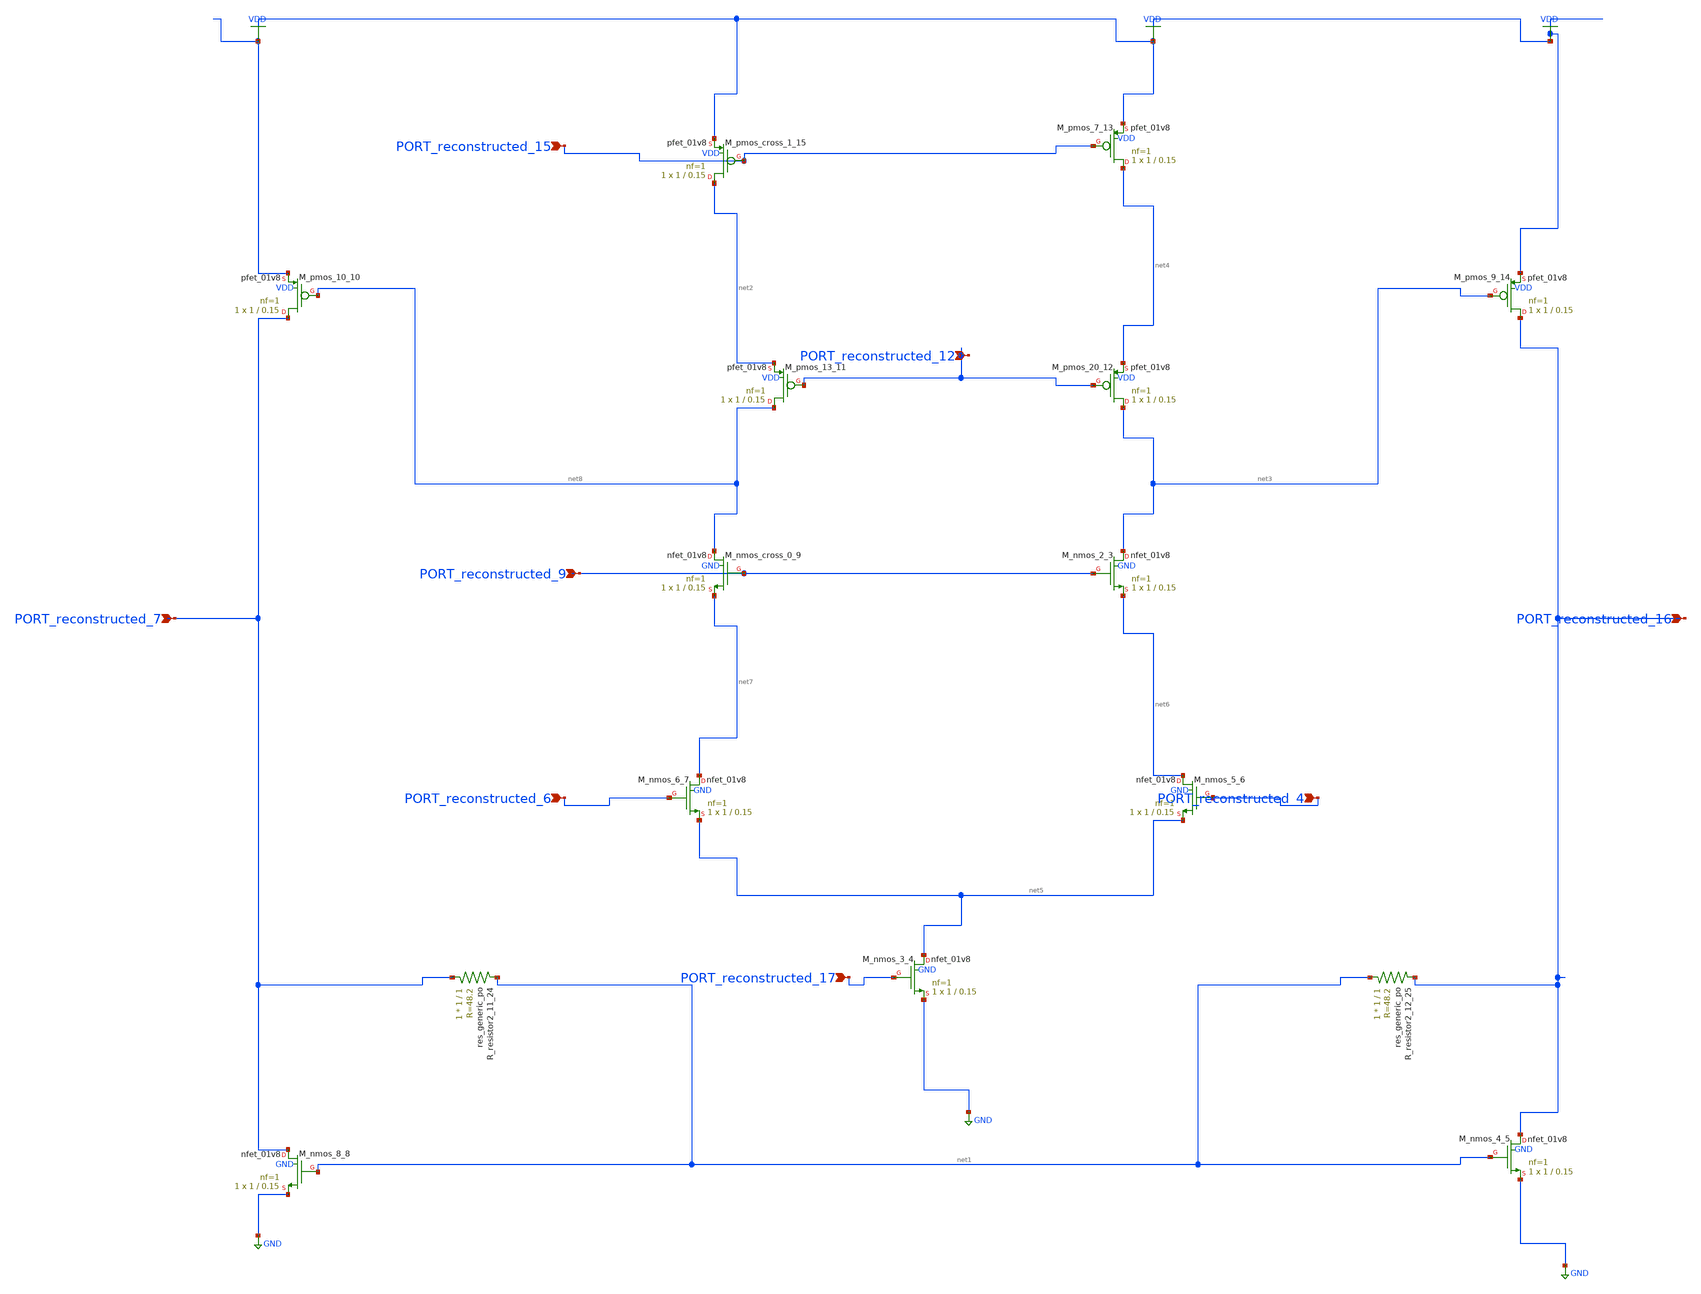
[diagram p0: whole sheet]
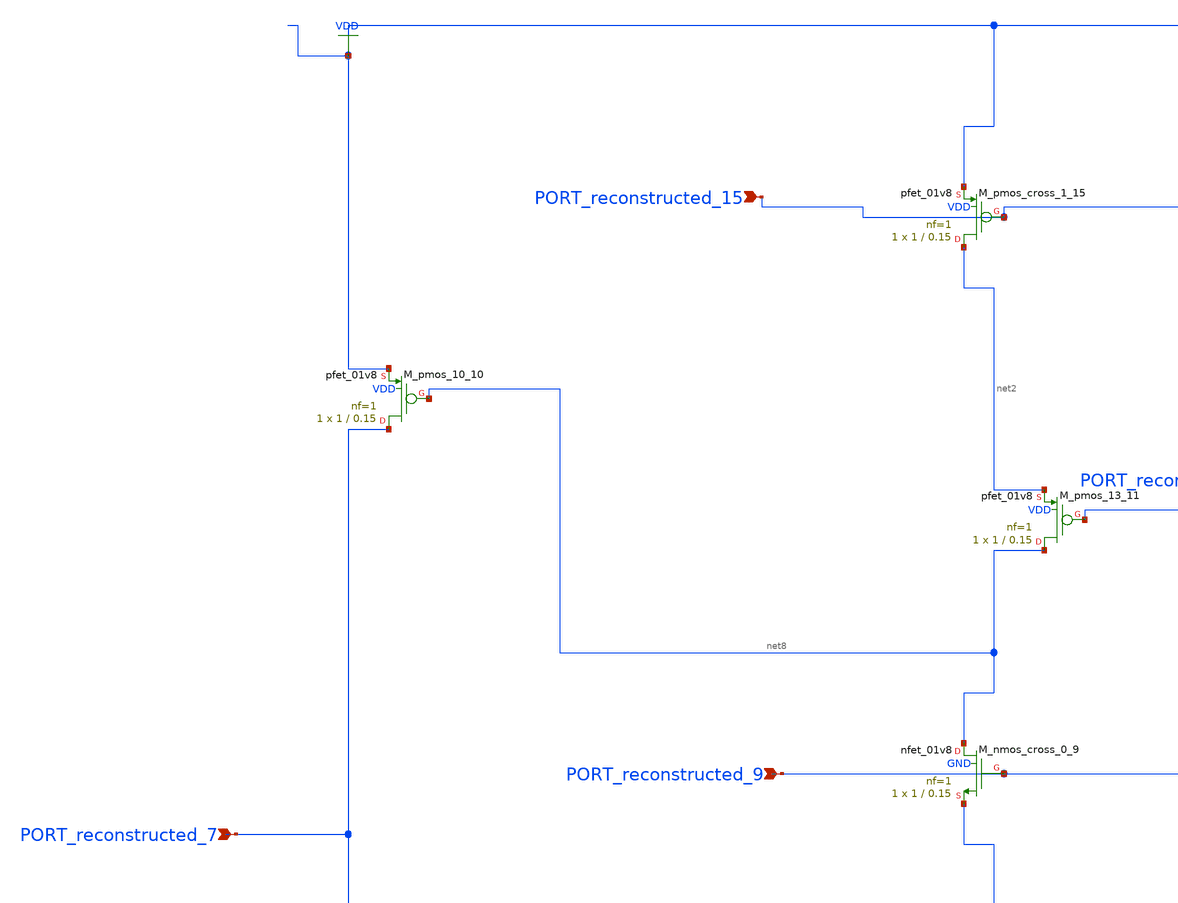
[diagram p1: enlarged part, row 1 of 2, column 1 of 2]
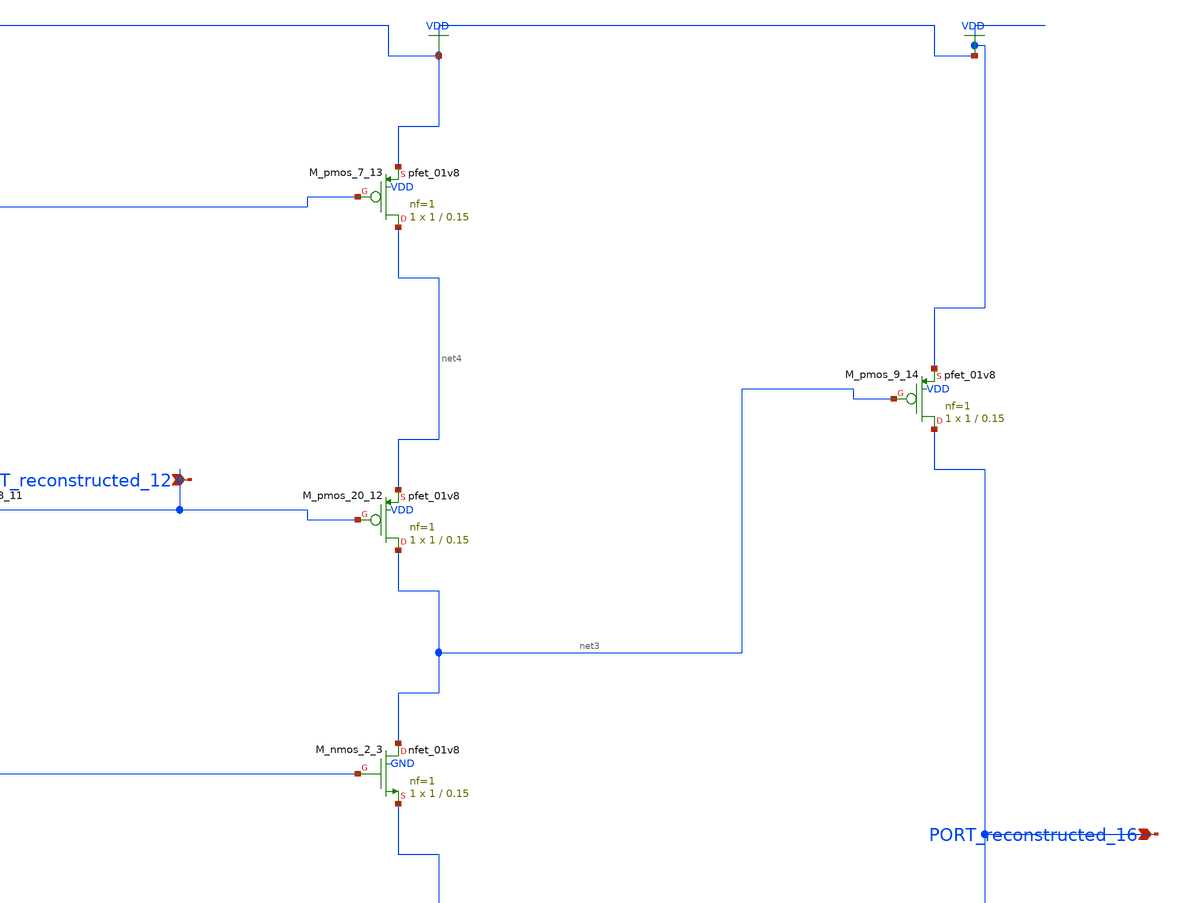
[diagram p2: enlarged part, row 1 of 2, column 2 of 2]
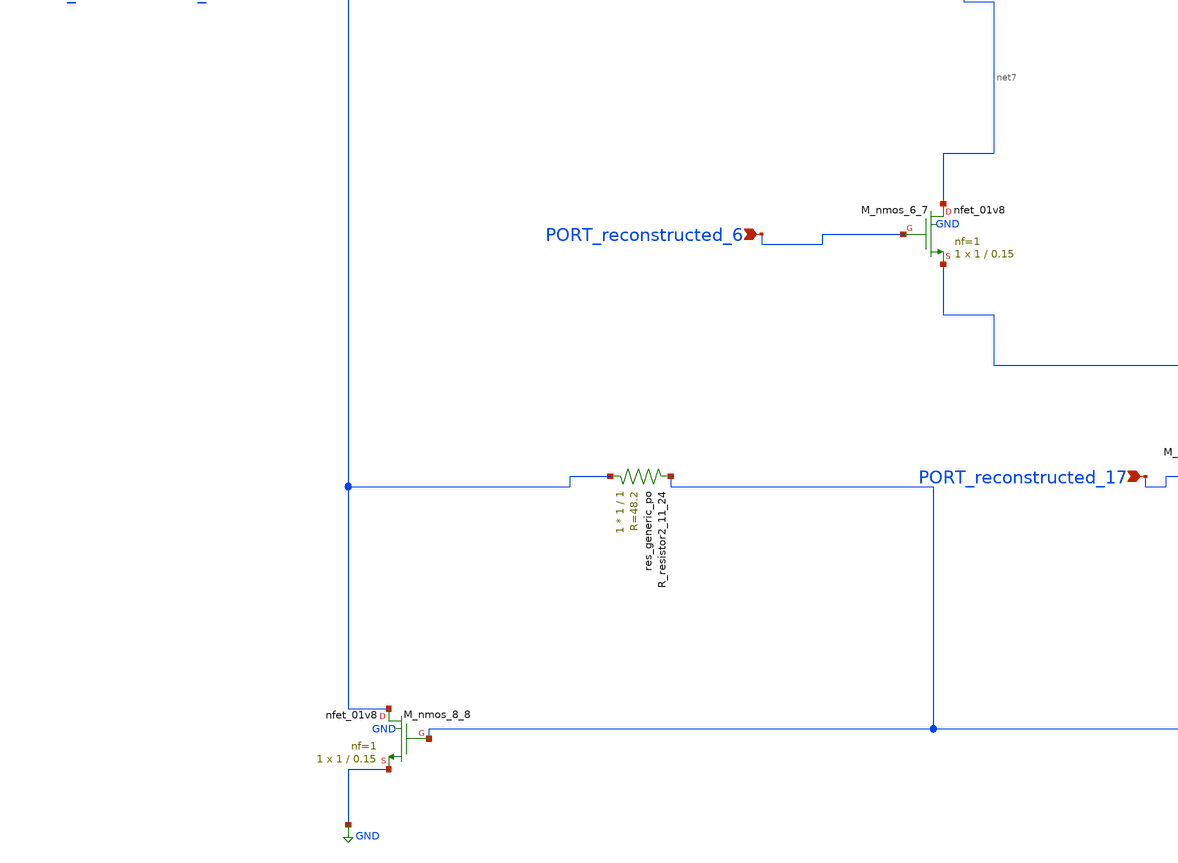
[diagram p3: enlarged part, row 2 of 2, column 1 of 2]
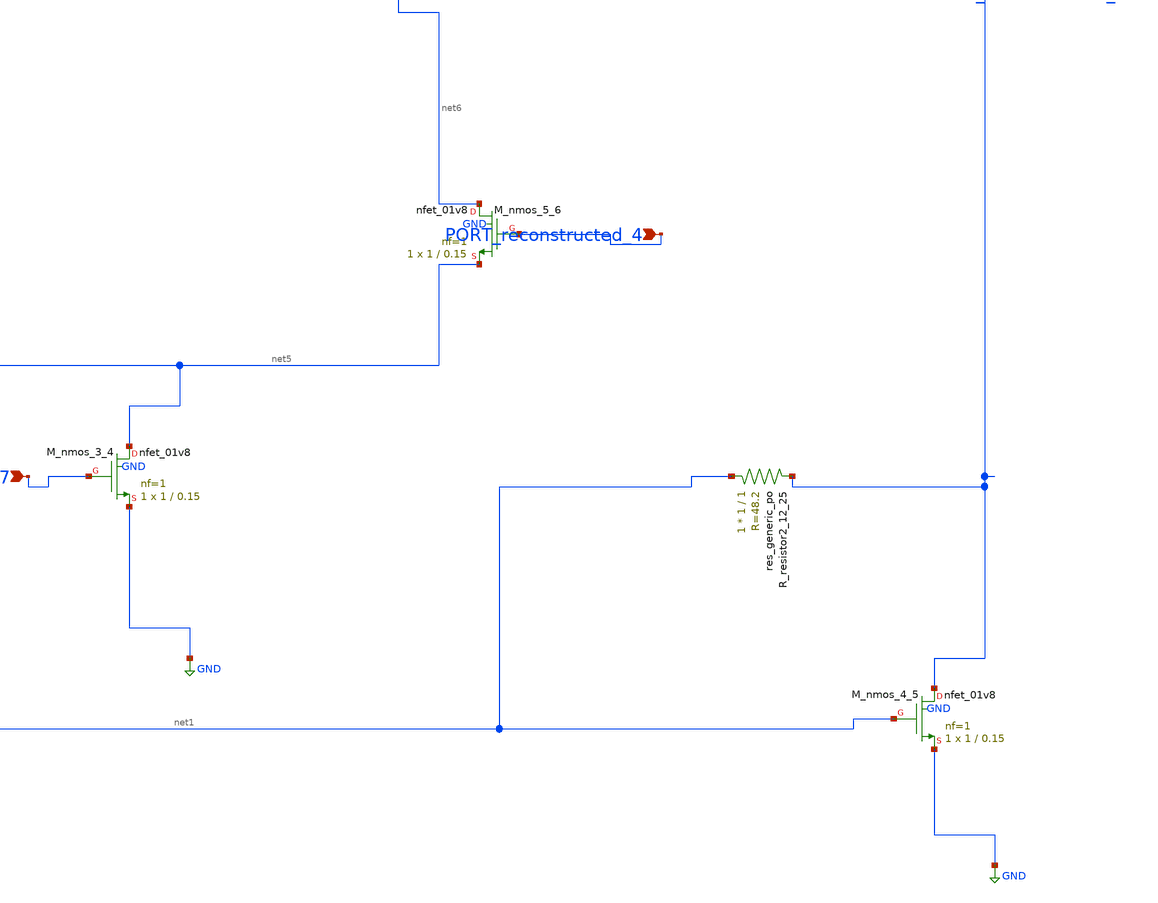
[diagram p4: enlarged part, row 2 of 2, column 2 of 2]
** sch_path: schematics/AMSNet/755.sch
**.subckt 755 PORT_reconstructed_4 PORT_reconstructed_16 PORT_reconstructed_7 PORT_reconstructed_6
*+ PORT_reconstructed_17 PORT_reconstructed_15 PORT_reconstructed_9 PORT_reconstructed_12
*.ipin PORT_reconstructed_4
*.ipin PORT_reconstructed_16
*.ipin PORT_reconstructed_7
*.ipin PORT_reconstructed_6
*.ipin PORT_reconstructed_17
*.ipin PORT_reconstructed_15
*.ipin PORT_reconstructed_9
*.ipin PORT_reconstructed_12
XM_nmos_2_3 net3 PORT_reconstructed_9 net6 GND sky130_fd_pr__nfet_01v8 L=0.15 W=1 nf=1 ad='int((1 + 1)/2) * 1 / 1 * 0.29'
+ as='int((1 + 2)/2) * 1 / 1 * 0.29' pd='2*int((1 + 1)/2) * (1 / 1 + 0.29)' ps='2*int((1 + 2)/2) * (1 / 1 + 0.29)'
+ nrd='0.29 / 1 ' nrs='0.29 / 1 ' sa=0 sb=0 sd=0 mult=1 m=1
XM_nmos_3_4 net5 PORT_reconstructed_17 GND GND sky130_fd_pr__nfet_01v8 L=0.15 W=1 nf=1 ad='int((1 + 1)/2) * 1 / 1 * 0.29'
+ as='int((1 + 2)/2) * 1 / 1 * 0.29' pd='2*int((1 + 1)/2) * (1 / 1 + 0.29)' ps='2*int((1 + 2)/2) * (1 / 1 + 0.29)'
+ nrd='0.29 / 1 ' nrs='0.29 / 1 ' sa=0 sb=0 sd=0 mult=1 m=1
XM_nmos_4_5 PORT_reconstructed_16 net1 GND GND sky130_fd_pr__nfet_01v8 L=0.15 W=1 nf=1 ad='int((1 + 1)/2) * 1 / 1 * 0.29'
+ as='int((1 + 2)/2) * 1 / 1 * 0.29' pd='2*int((1 + 1)/2) * (1 / 1 + 0.29)' ps='2*int((1 + 2)/2) * (1 / 1 + 0.29)'
+ nrd='0.29 / 1 ' nrs='0.29 / 1 ' sa=0 sb=0 sd=0 mult=1 m=1
XM_nmos_5_6 net6 PORT_reconstructed_4 net5 GND sky130_fd_pr__nfet_01v8 L=0.15 W=1 nf=1 ad='int((1 + 1)/2) * 1 / 1 * 0.29'
+ as='int((1 + 2)/2) * 1 / 1 * 0.29' pd='2*int((1 + 1)/2) * (1 / 1 + 0.29)' ps='2*int((1 + 2)/2) * (1 / 1 + 0.29)'
+ nrd='0.29 / 1 ' nrs='0.29 / 1 ' sa=0 sb=0 sd=0 mult=1 m=1
XM_nmos_6_7 net7 PORT_reconstructed_6 net5 GND sky130_fd_pr__nfet_01v8 L=0.15 W=1 nf=1 ad='int((1 + 1)/2) * 1 / 1 * 0.29'
+ as='int((1 + 2)/2) * 1 / 1 * 0.29' pd='2*int((1 + 1)/2) * (1 / 1 + 0.29)' ps='2*int((1 + 2)/2) * (1 / 1 + 0.29)'
+ nrd='0.29 / 1 ' nrs='0.29 / 1 ' sa=0 sb=0 sd=0 mult=1 m=1
XM_nmos_8_8 PORT_reconstructed_7 net1 GND GND sky130_fd_pr__nfet_01v8 L=0.15 W=1 nf=1 ad='int((1 + 1)/2) * 1 / 1 * 0.29'
+ as='int((1 + 2)/2) * 1 / 1 * 0.29' pd='2*int((1 + 1)/2) * (1 / 1 + 0.29)' ps='2*int((1 + 2)/2) * (1 / 1 + 0.29)'
+ nrd='0.29 / 1 ' nrs='0.29 / 1 ' sa=0 sb=0 sd=0 mult=1 m=1
XM_nmos_cross_0_9 net8 PORT_reconstructed_9 net7 GND sky130_fd_pr__nfet_01v8 L=0.15 W=1 nf=1 ad='int((1 + 1)/2) * 1 / 1 * 0.29'
+ as='int((1 + 2)/2) * 1 / 1 * 0.29' pd='2*int((1 + 1)/2) * (1 / 1 + 0.29)' ps='2*int((1 + 2)/2) * (1 / 1 + 0.29)'
+ nrd='0.29 / 1 ' nrs='0.29 / 1 ' sa=0 sb=0 sd=0 mult=1 m=1
XM_pmos_10_10 PORT_reconstructed_7 net8 VDD VDD sky130_fd_pr__pfet_01v8 L=0.15 W=1 nf=1 ad='int((1 + 1)/2) * 1 / 1 * 0.29'
+ as='int((1 + 2)/2) * 1 / 1 * 0.29' pd='2*int((1 + 1)/2) * (1 / 1 + 0.29)' ps='2*int((1 + 2)/2) * (1 / 1 + 0.29)'
+ nrd='0.29 / 1 ' nrs='0.29 / 1 ' sa=0 sb=0 sd=0 mult=1 m=1
XM_pmos_13_11 net8 PORT_reconstructed_12 net2 VDD sky130_fd_pr__pfet_01v8 L=0.15 W=1 nf=1 ad='int((1 + 1)/2) * 1 / 1 * 0.29'
+ as='int((1 + 2)/2) * 1 / 1 * 0.29' pd='2*int((1 + 1)/2) * (1 / 1 + 0.29)' ps='2*int((1 + 2)/2) * (1 / 1 + 0.29)'
+ nrd='0.29 / 1 ' nrs='0.29 / 1 ' sa=0 sb=0 sd=0 mult=1 m=1
XM_pmos_20_12 net3 PORT_reconstructed_12 net4 VDD sky130_fd_pr__pfet_01v8 L=0.15 W=1 nf=1 ad='int((1 + 1)/2) * 1 / 1 * 0.29'
+ as='int((1 + 2)/2) * 1 / 1 * 0.29' pd='2*int((1 + 1)/2) * (1 / 1 + 0.29)' ps='2*int((1 + 2)/2) * (1 / 1 + 0.29)'
+ nrd='0.29 / 1 ' nrs='0.29 / 1 ' sa=0 sb=0 sd=0 mult=1 m=1
XM_pmos_7_13 net4 PORT_reconstructed_15 VDD VDD sky130_fd_pr__pfet_01v8 L=0.15 W=1 nf=1 ad='int((1 + 1)/2) * 1 / 1 * 0.29'
+ as='int((1 + 2)/2) * 1 / 1 * 0.29' pd='2*int((1 + 1)/2) * (1 / 1 + 0.29)' ps='2*int((1 + 2)/2) * (1 / 1 + 0.29)'
+ nrd='0.29 / 1 ' nrs='0.29 / 1 ' sa=0 sb=0 sd=0 mult=1 m=1
XM_pmos_9_14 PORT_reconstructed_16 net3 VDD VDD sky130_fd_pr__pfet_01v8 L=0.15 W=1 nf=1 ad='int((1 + 1)/2) * 1 / 1 * 0.29'
+ as='int((1 + 2)/2) * 1 / 1 * 0.29' pd='2*int((1 + 1)/2) * (1 / 1 + 0.29)' ps='2*int((1 + 2)/2) * (1 / 1 + 0.29)'
+ nrd='0.29 / 1 ' nrs='0.29 / 1 ' sa=0 sb=0 sd=0 mult=1 m=1
XM_pmos_cross_1_15 net2 PORT_reconstructed_15 VDD VDD sky130_fd_pr__pfet_01v8 L=0.15 W=1 nf=1 ad='int((1 + 1)/2) * 1 / 1 * 0.29'
+ as='int((1 + 2)/2) * 1 / 1 * 0.29' pd='2*int((1 + 1)/2) * (1 / 1 + 0.29)' ps='2*int((1 + 2)/2) * (1 / 1 + 0.29)'
+ nrd='0.29 / 1 ' nrs='0.29 / 1 ' sa=0 sb=0 sd=0 mult=1 m=1
XR_resistor2_11_24 PORT_reconstructed_7 net1 sky130_fd_pr__res_generic_po W=1 L=1 m=1
XR_resistor2_12_25 net1 PORT_reconstructed_16 sky130_fd_pr__res_generic_po W=1 L=1 m=1
**.ends
.GLOBAL GND
.GLOBAL VDD
.end
